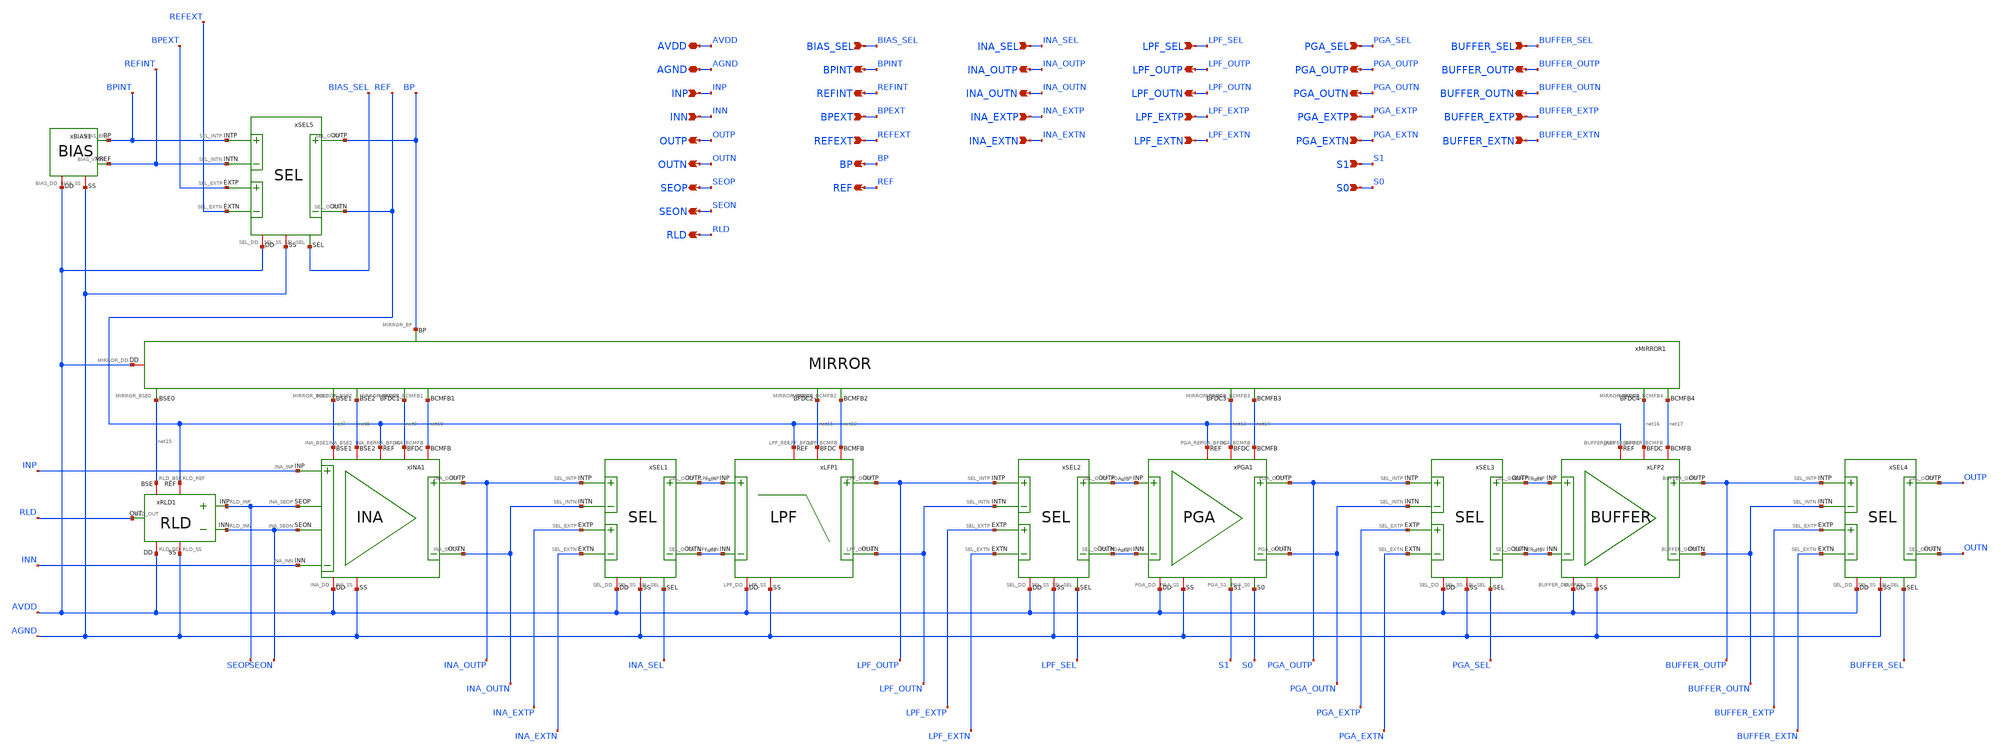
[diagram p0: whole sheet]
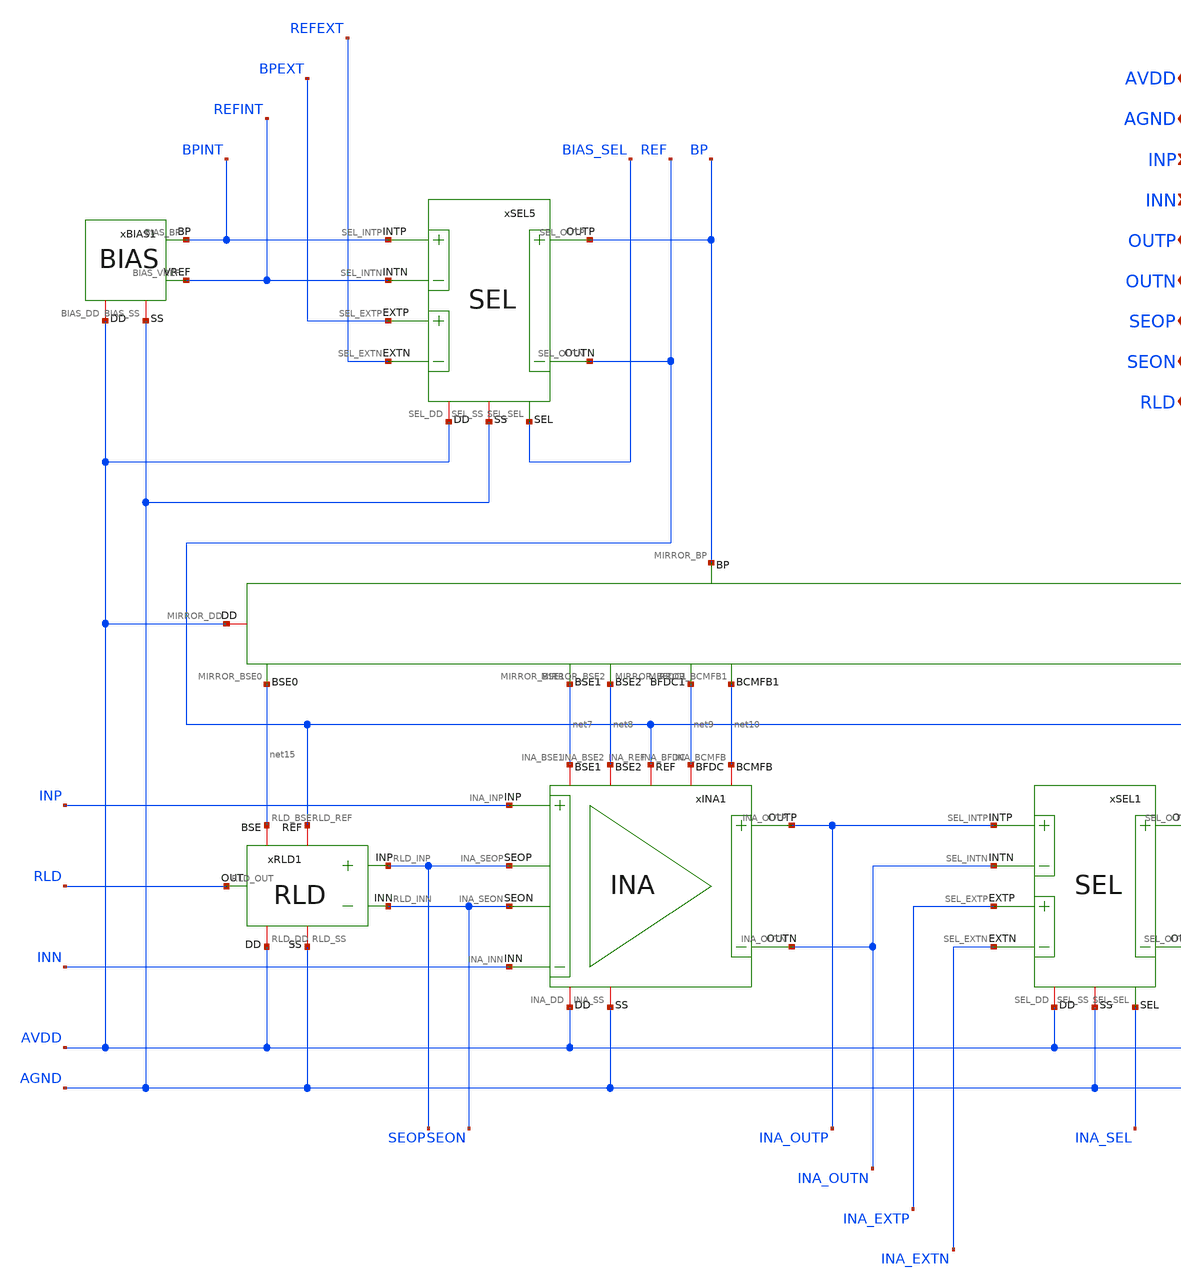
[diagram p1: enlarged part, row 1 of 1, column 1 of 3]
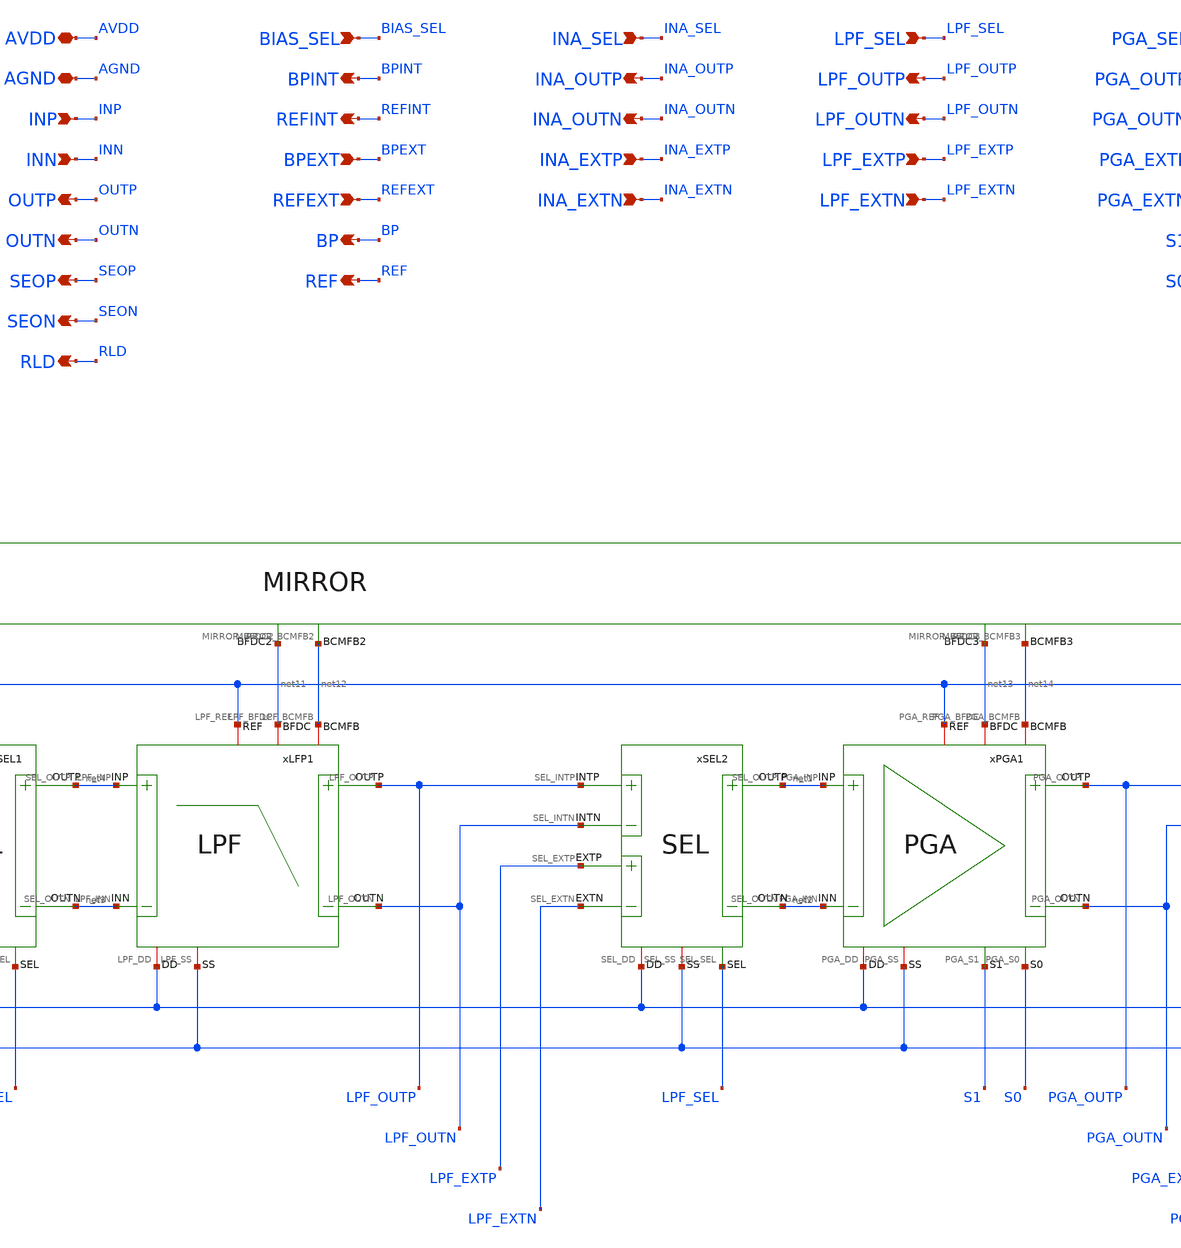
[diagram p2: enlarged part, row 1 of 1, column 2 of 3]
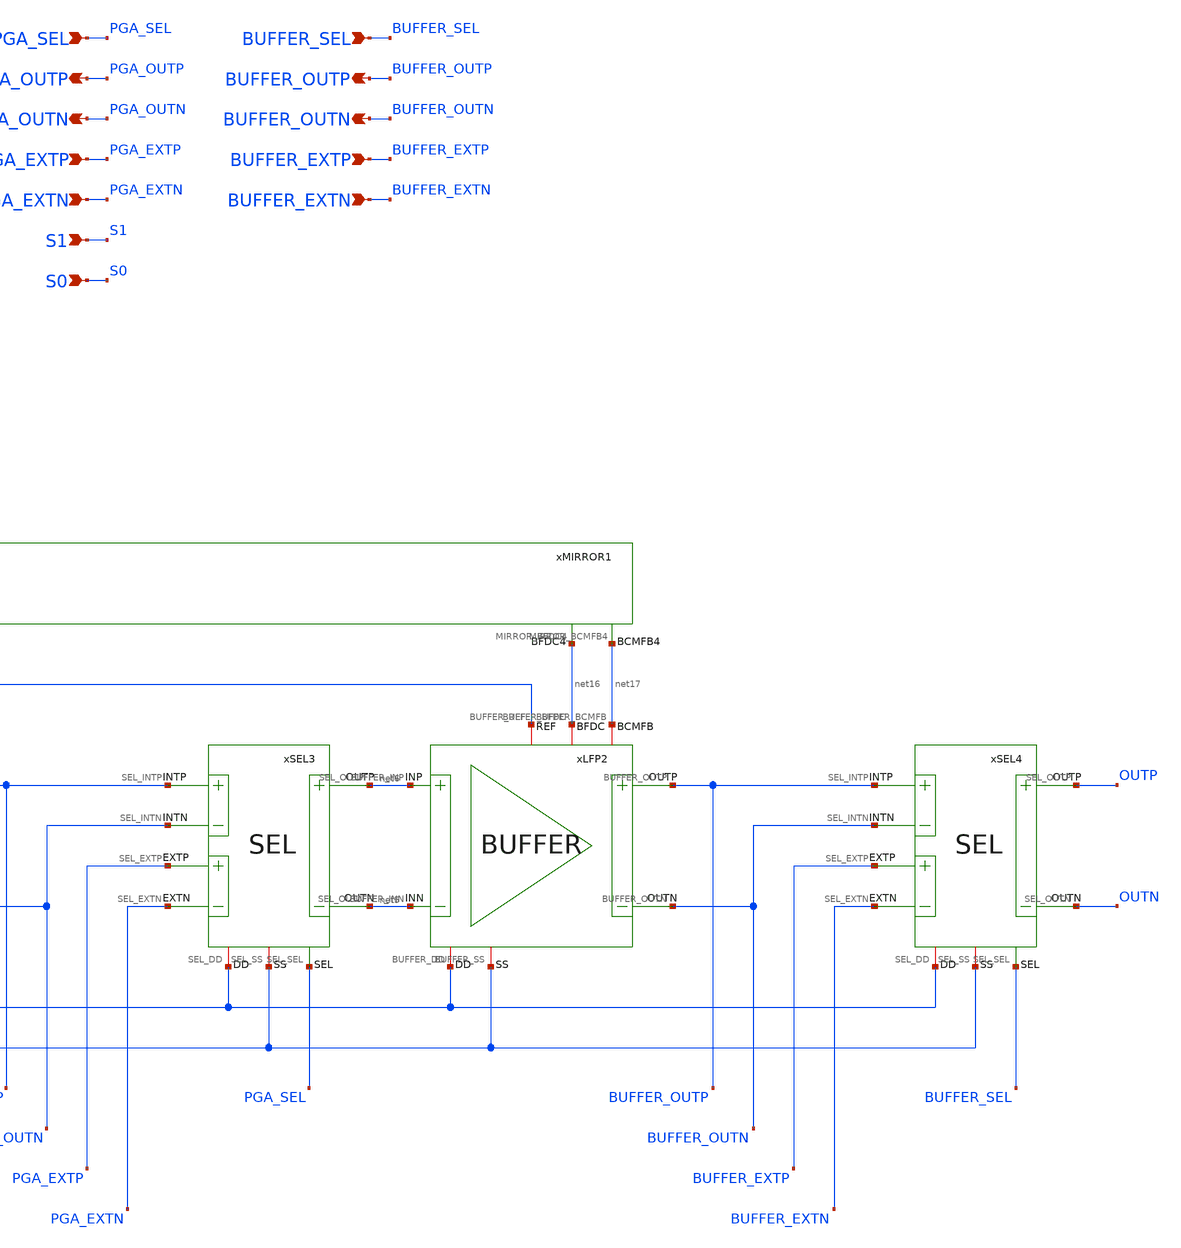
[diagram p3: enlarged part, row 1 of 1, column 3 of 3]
** sch_path: Design_Files/IC Design/Schematic/AFE/AFE.sch
**.subckt AFE INA_OUTP INA_OUTN INA_EXTP INA_EXTN LPF_OUTP LPF_OUTN LPF_EXTP LPF_EXTN PGA_OUTP
*+ PGA_OUTN PGA_EXTP PGA_EXTN BUFFER_OUTP BUFFER_OUTN BUFFER_EXTP BUFFER_EXTN AVDD AGND SEOP SEON RLD INP INN
*+ BPINT REFINT BPEXT REFEXT BIAS_SEL BP REF INA_SEL LPF_SEL PGA_SEL S1 S0 BUFFER_SEL OUTP OUTN
*.opin INA_OUTP
*.opin INA_OUTN
*.ipin INA_EXTP
*.ipin INA_EXTN
*.opin LPF_OUTP
*.opin LPF_OUTN
*.ipin LPF_EXTP
*.ipin LPF_EXTN
*.opin PGA_OUTP
*.opin PGA_OUTN
*.ipin PGA_EXTP
*.ipin PGA_EXTN
*.opin BUFFER_OUTP
*.opin BUFFER_OUTN
*.ipin BUFFER_EXTP
*.ipin BUFFER_EXTN
*.iopin AVDD
*.iopin AGND
*.opin SEOP
*.opin SEON
*.opin RLD
*.ipin INP
*.ipin INN
*.opin BPINT
*.opin REFINT
*.ipin BPEXT
*.ipin REFEXT
*.ipin BIAS_SEL
*.opin BP
*.opin REF
*.ipin INA_SEL
*.ipin LPF_SEL
*.ipin PGA_SEL
*.ipin S1
*.ipin S0
*.ipin BUFFER_SEL
*.opin OUTP
*.opin OUTN
xLFP1 AVDD AGND net4 net3 LPF_OUTN net11 LPF_OUTP net12 REF LPF
xPGA1 AVDD AGND net1 net2 PGA_OUTN net13 PGA_OUTP net14 REF S1 S0 PGA
xSEL1 AVDD AGND INA_OUTP INA_OUTN net3 net4 INA_EXTP INA_EXTN INA_SEL SEL
xINA1 AVDD AGND INP INN INA_OUTN net9 INA_OUTP net10 REF SEON SEOP net7 net8 INA
xSEL2 AVDD AGND LPF_OUTP LPF_OUTN net2 net1 LPF_EXTP LPF_EXTN LPF_SEL SEL
xSEL3 AVDD AGND PGA_OUTP PGA_OUTN net5 net6 PGA_EXTP PGA_EXTN PGA_SEL SEL
xSEL4 AVDD AGND BUFFER_OUTP BUFFER_OUTN OUTN OUTP BUFFER_EXTP BUFFER_EXTN BUFFER_SEL SEL
xLFP2 AVDD AGND net6 net5 BUFFER_OUTN net16 BUFFER_OUTP net17 REF BUFFER
xRLD1 AVDD AGND SEOP SEON RLD REF net15 RLD
xBIAS1 AVDD AGND BPINT REFINT BIAS
xSEL5 AVDD AGND BPINT REFINT REF BP BPEXT REFEXT BIAS_SEL SEL
xMIRROR1 AVDD BP net15 net7 net8 net9 net11 net13 net16 net10 net12 net14 net17 MIRROR
**.ends
.end
